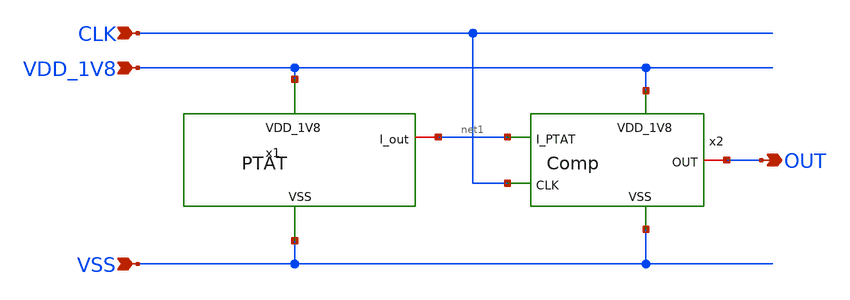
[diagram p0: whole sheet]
** sch_path: design/JNW_GR04_SKY130A/PTAT_TO_COMP.sch
**.subckt PTAT_TO_COMP VDD_1V8 VSS OUT CLK
*.ipin VDD_1V8
*.ipin VSS
*.opin OUT
*.ipin CLK
x1 VDD_1V8 net1 VSS PTAT
x2 VDD_1V8 OUT net1 VSS CLK Comp
**.ends
.end
